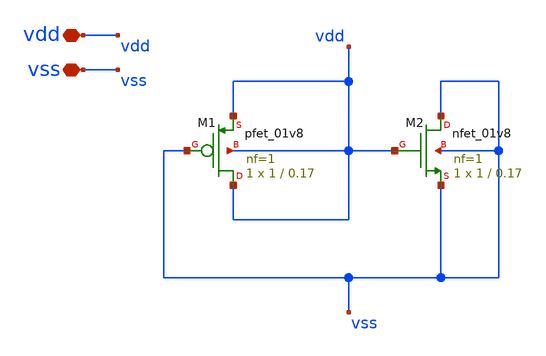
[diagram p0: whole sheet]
** sch_path: xschem/decap/decap.sch
**.subckt decap vdd vss
*.iopin vdd
*.iopin vss
XM2 vss vdd vss vss sky130_fd_pr__nfet_01v8 L=0.17 W=1 nf=1 ad={int((nf+1)/2) * W/nf * 0.29} as={int((nf+2)/2) * W/nf * 0.29}
+ pd={2*int((nf+1)/2) * (W/nf + 0.29)} ps={2*int((nf+2)/2) * (W/nf + 0.29)} nrd={0.29 / W} nrs={0.29 / W}
+ sa=0 sb=0 sd=0 mult=1 m=1
XM1 vdd vss vdd vdd sky130_fd_pr__pfet_01v8 L=0.17 W=1 nf=1 ad={int((nf+1)/2) * W/nf * 0.29} as={int((nf+2)/2) * W/nf * 0.29}
+ pd={2*int((nf+1)/2) * (W/nf + 0.29)} ps={2*int((nf+2)/2) * (W/nf + 0.29)} nrd={0.29 / W} nrs={0.29 / W}
+ sa=0 sb=0 sd=0 mult=1 m=1
**.ends
.end
